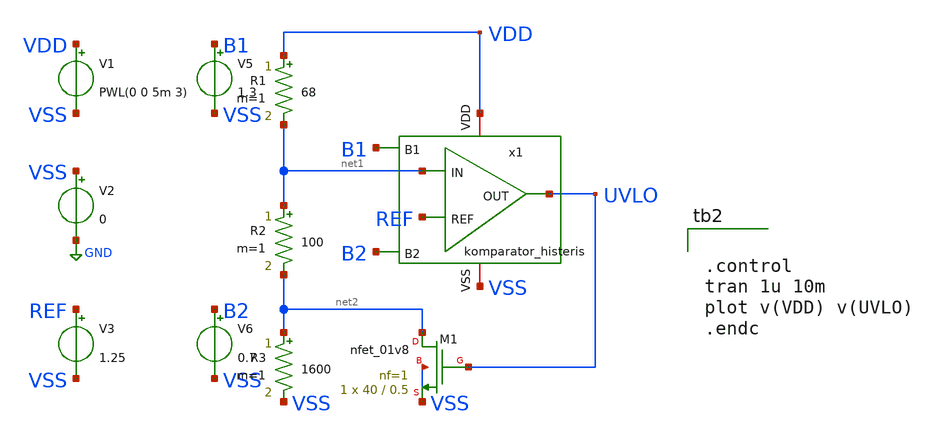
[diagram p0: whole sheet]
** sch_path: uvlo/uvlo_tb_tran.sch
**.subckt uvlo_tb_tran
x1 VDD REF net1 UVLO B1 B2 VSS komparator_histeris
V1 VDD VSS PWL(0 0 5m 3)
V2 VSS GND 0
V3 REF VSS 1.25
V5 B1 VSS 1.3
V6 B2 VSS 0.7
R1 VDD net1 68 m=1
R2 net1 net2 100 m=1
R3 net2 VSS 1600 m=1
XM1 net2 UVLO VSS VSS sky130_fd_pr__nfet_01v8 L=0.5 W=40 nf=1 ad='int((1 + 1)/2) * 40 / 1 * 0.29' as='int((1 + 2)/2) * 40 / 1 * 0.29'
+ pd='2*int((1 + 1)/2) * (40 / 1 + 0.29)' ps='2*int((1 + 2)/2) * (40 / 1 + 0.29)' nrd='0.29 / 40 ' nrs='0.29 / 40 '
+ sa=0 sb=0 sd=0 mult=1 m=1
**** begin user architecture code


.control
tran 1u 10m
plot v(VDD) v(UVLO)
.endc



** opencircuitdesign pdks install
.lib $::SKYWATER_MODELS/sky130.lib.spice tt

**** end user architecture code
**.ends

* expanding   symbol:  komparator_histeris.sym # of pins=7
** sym_path: cmos_comparator/komparator_histeris.sym
** sch_path: cmos_comparator/komparator_histeris.sch
.subckt komparator_histeris VDD REF IN OUT B1 B2 VSS
*.iopin VDD
*.iopin VSS
*.iopin IN
*.iopin REF
*.iopin B2
*.iopin B1
*.iopin OUT
XM1 net1 net1 VDD VDD sky130_fd_pr__pfet_01v8 L=0.75 W=3.9 nf=1 ad='int((1 + 1)/2) * 3.9 / 1 * 0.29'
+ as='int((1 + 2)/2) * 3.9 / 1 * 0.29' pd='2*int((1 + 1)/2) * (3.9 / 1 + 0.29)' ps='2*int((1 + 2)/2) * (3.9 / 1 + 0.29)'
+ nrd='0.29 / 3.9 ' nrs='0.29 / 3.9 ' sa=0 sb=0 sd=0 mult=1 m=1
XM2 net1 REF net3 net3 sky130_fd_pr__nfet_01v8 L=0.5 W=3.4 nf=1 ad='int((1 + 1)/2) * 3.4 / 1 * 0.29'
+ as='int((1 + 2)/2) * 3.4 / 1 * 0.29' pd='2*int((1 + 1)/2) * (3.4 / 1 + 0.29)' ps='2*int((1 + 2)/2) * (3.4 / 1 + 0.29)'
+ nrd='0.29 / 3.4 ' nrs='0.29 / 3.4 ' sa=0 sb=0 sd=0 mult=1 m=1
XM3 net2 net1 VDD VDD sky130_fd_pr__pfet_01v8 L=0.75 W=3.9 nf=1 ad='int((1 + 1)/2) * 3.9 / 1 * 0.29'
+ as='int((1 + 2)/2) * 3.9 / 1 * 0.29' pd='2*int((1 + 1)/2) * (3.9 / 1 + 0.29)' ps='2*int((1 + 2)/2) * (3.9 / 1 + 0.29)'
+ nrd='0.29 / 3.9 ' nrs='0.29 / 3.9 ' sa=0 sb=0 sd=0 mult=1 m=1
XM4 net4 net1 VDD VDD sky130_fd_pr__pfet_01v8 L=0.75 W=3.9 nf=1 ad='int((1 + 1)/2) * 3.9 / 1 * 0.29'
+ as='int((1 + 2)/2) * 3.9 / 1 * 0.29' pd='2*int((1 + 1)/2) * (3.9 / 1 + 0.29)' ps='2*int((1 + 2)/2) * (3.9 / 1 + 0.29)'
+ nrd='0.29 / 3.9 ' nrs='0.29 / 3.9 ' sa=0 sb=0 sd=0 mult=1 m=1
XM5 net1 net2 VDD VDD sky130_fd_pr__pfet_01v8 L=0.15 W=1 nf=1 ad='int((1 + 1)/2) * 1 / 1 * 0.29' as='int((1 + 2)/2) * 1 / 1 * 0.29'
+ pd='2*int((1 + 1)/2) * (1 / 1 + 0.29)' ps='2*int((1 + 2)/2) * (1 / 1 + 0.29)' nrd='0.29 / 1 ' nrs='0.29 / 1 '
+ sa=0 sb=0 sd=0 mult=1 m=1
XM6 net2 net2 VDD VDD sky130_fd_pr__pfet_01v8 L=0.75 W=3.9 nf=1 ad='int((1 + 1)/2) * 3.9 / 1 * 0.29'
+ as='int((1 + 2)/2) * 3.9 / 1 * 0.29' pd='2*int((1 + 1)/2) * (3.9 / 1 + 0.29)' ps='2*int((1 + 2)/2) * (3.9 / 1 + 0.29)'
+ nrd='0.29 / 3.9 ' nrs='0.29 / 3.9 ' sa=0 sb=0 sd=0 mult=1 m=1
XM7 OUT net2 VDD VDD sky130_fd_pr__pfet_01v8 L=0.75 W=3.9 nf=1 ad='int((1 + 1)/2) * 3.9 / 1 * 0.29' as='int((1 + 2)/2) * 3.9 / 1 * 0.29'
+ pd='2*int((1 + 1)/2) * (3.9 / 1 + 0.29)' ps='2*int((1 + 2)/2) * (3.9 / 1 + 0.29)' nrd='0.29 / 3.9 ' nrs='0.29 / 3.9 '
+ sa=0 sb=0 sd=0 mult=1 m=1
XM8 net2 IN net3 net3 sky130_fd_pr__nfet_01v8 L=0.5 W=3.4 nf=1 ad='int((1 + 1)/2) * 3.4 / 1 * 0.29' as='int((1 + 2)/2) * 3.4 / 1 * 0.29'
+ pd='2*int((1 + 1)/2) * (3.4 / 1 + 0.29)' ps='2*int((1 + 2)/2) * (3.4 / 1 + 0.29)' nrd='0.29 / 3.4 ' nrs='0.29 / 3.4 '
+ sa=0 sb=0 sd=0 mult=1 m=1
XM9 net3 B1 VSS VSS sky130_fd_pr__nfet_01v8 L=0.75 W=2.1 nf=1 ad='int((1 + 1)/2) * 2.1 / 1 * 0.29' as='int((1 + 2)/2) * 2.1 / 1 * 0.29'
+ pd='2*int((1 + 1)/2) * (2.1 / 1 + 0.29)' ps='2*int((1 + 2)/2) * (2.1 / 1 + 0.29)' nrd='0.29 / 2.1 ' nrs='0.29 / 2.1 '
+ sa=0 sb=0 sd=0 mult=1 m=1
XM10 OUT B2 VSS VSS sky130_fd_pr__nfet_01v8 L=0.75 W=2.1 nf=1 ad='int((1 + 1)/2) * 2.1 / 1 * 0.29' as='int((1 + 2)/2) * 2.1 / 1 * 0.29'
+ pd='2*int((1 + 1)/2) * (2.1 / 1 + 0.29)' ps='2*int((1 + 2)/2) * (2.1 / 1 + 0.29)' nrd='0.29 / 2.1 ' nrs='0.29 / 2.1 '
+ sa=0 sb=0 sd=0 mult=1 m=1
XM11 net4 B2 VSS VSS sky130_fd_pr__nfet_01v8 L=0.75 W=2.1 nf=1 ad='int((1 + 1)/2) * 2.1 / 1 * 0.29' as='int((1 + 2)/2) * 2.1 / 1 * 0.29'
+ pd='2*int((1 + 1)/2) * (2.1 / 1 + 0.29)' ps='2*int((1 + 2)/2) * (2.1 / 1 + 0.29)' nrd='0.29 / 2.1 ' nrs='0.29 / 2.1 '
+ sa=0 sb=0 sd=0 mult=1 m=1
.ends

.GLOBAL GND
.end
